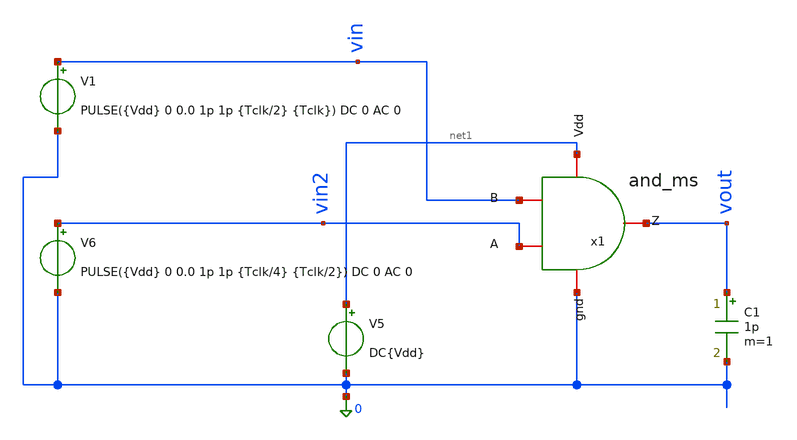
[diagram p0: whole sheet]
** sch_path: verification/testbenches/tb_and_ms.sch
**.subckt tb_and_ms
V5 net1 0 DC{Vdd}
V6 vin2 0 PULSE({Vdd} 0 0.0 1p 1p {Tclk/4} {Tclk/2}) DC 0 AC 0
V1 vin 0 PULSE({Vdd} 0 0.0 1p 1p {Tclk/2} {Tclk}) DC 0 AC 0
C1 vout 0 1p m=1
x1 vin2 vin vout 0 net1 and_ms
**** begin user architecture code


* Circuit Parameters
.param Vdd = 1.2
.param Tclk = 20n
.options TEMP = 27.0
* Include Models - IHP SG13G2
.lib cornerMOSlv.lib mos_tt
* OP Parameters & Singals to save
.save all
*Simulations
.control
tran 0.01u 100n
setplot tran1
plot v(vin) v(vin2)+1.2 v(vout)+2.4
reset
dc V6 0 1.2 0.01
dc V1 0 1.2 0.01
setplot dc
plot vin vout ylabel vout xlabel vin
set filetype = ascii
write dcsweep.raw
.endc
.end


**** end user architecture code
**.ends

* expanding   symbol:  blocks/and_ms/schematic/and_ms.sym # of pins=5
** sym_path: design/blocks/and_ms/schematic/and_ms.sym
** sch_path: design/blocks/and_ms/schematic/and_ms.sch
.subckt and_ms A B Z gnd Vdd
*.iopin A
*.iopin B
*.iopin Vdd
*.iopin Z
*.iopin gnd
XM2 net1 A net2 gnd sg13_lv_nmos w=1.5u l=0.15u ng=1 m=1 mm_ok=1
XM3 net2 B gnd gnd sg13_lv_nmos w=1.5u l=0.15u ng=1 m=1 mm_ok=1
XM5 Z net1 gnd gnd sg13_lv_nmos w=0.75u l=0.15u ng=1 m=1 mm_ok=1
XM0 net1 A Vdd Vdd sg13_lv_pmos w=1.5u l=0.15u ng=1 m=1 mm_ok=1
XM1 Vdd B net1 Vdd sg13_lv_pmos w=1.5u l=0.15u ng=1 m=1 mm_ok=1
XM4 Z net1 Vdd Vdd sg13_lv_pmos w=1.5u l=0.15u ng=1 m=1 mm_ok=1
.ends

.end
